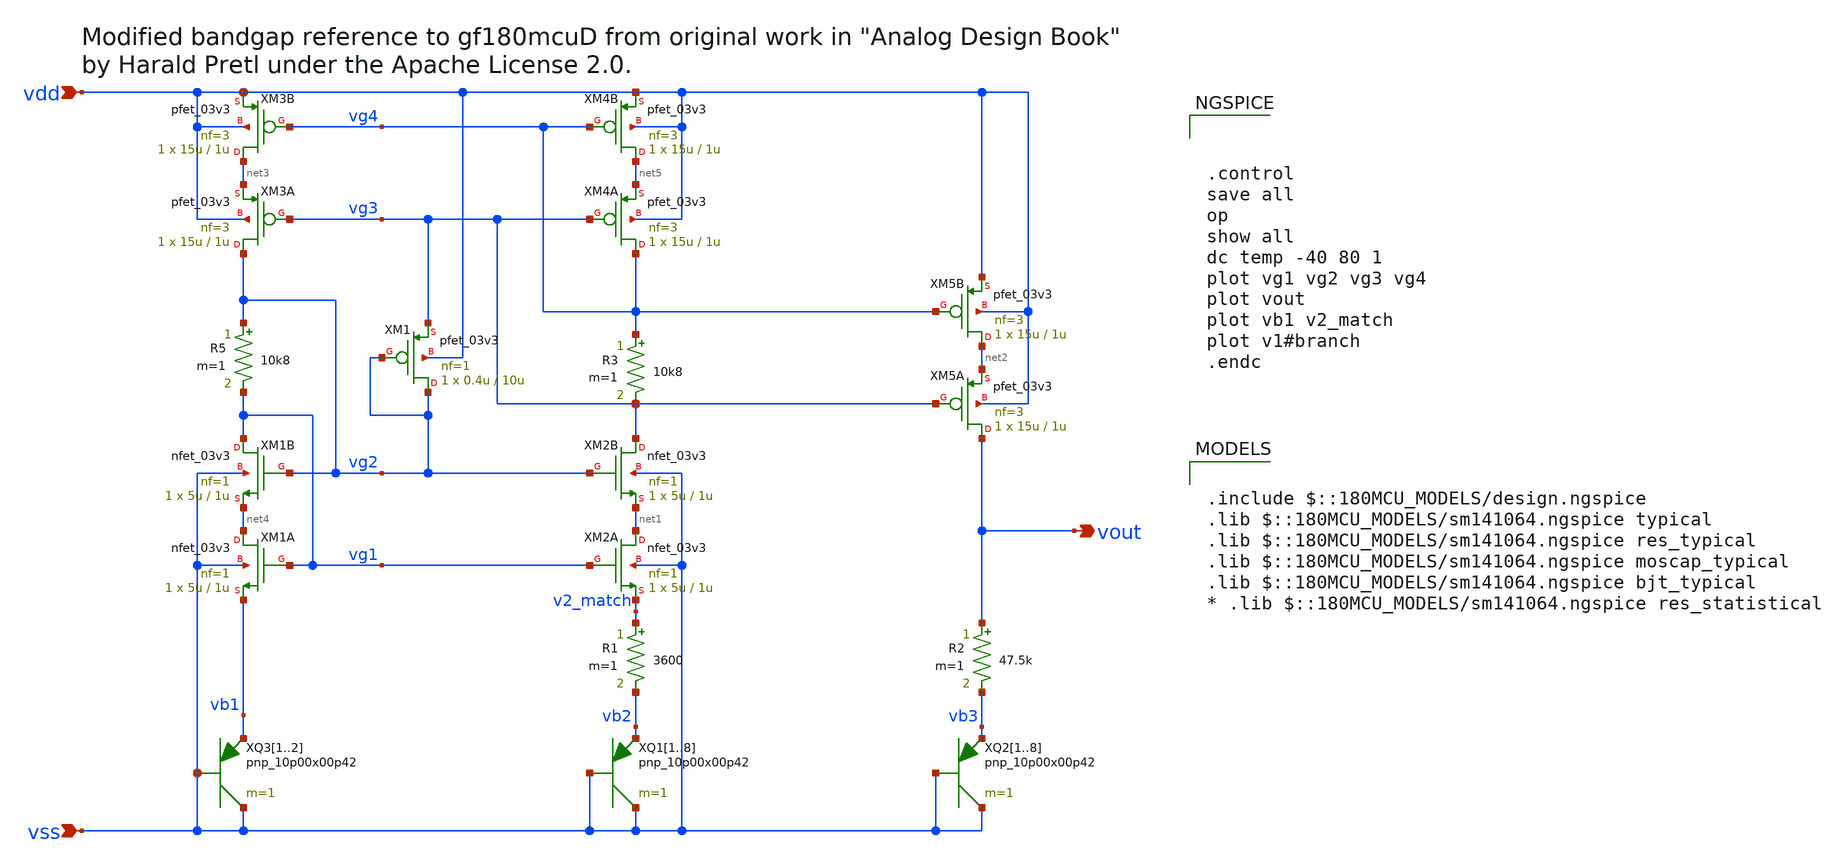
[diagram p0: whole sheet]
** sch_path: designs/switch_matrix_gf180mcu_9t5v0-main/designs/libs/core_analog/vref/voltage_reference.sch
* by Harald Pretl under the Apache License 2.0.
**.subckt voltage_reference vdd vout vss
*.ipin vdd
*.opin vout
*.ipin vss
XM1B vg1 vg2 net4 vss nfet_03v3 L=1u W=5u nf=1 ad='int((nf+1)/2) * W/nf * 0.18u' as='int((nf+2)/2) * W/nf * 0.18u'
+ pd='2*int((nf+1)/2) * (W/nf + 0.18u)' ps='2*int((nf+2)/2) * (W/nf + 0.18u)' nrd='0.18u / W' nrs='0.18u / W'
+ sa=0 sb=0 sd=0 m=1
XM1A net4 vg1 vb1 vss nfet_03v3 L=1u W=5u nf=1 ad='int((nf+1)/2) * W/nf * 0.18u' as='int((nf+2)/2) * W/nf * 0.18u'
+ pd='2*int((nf+1)/2) * (W/nf + 0.18u)' ps='2*int((nf+2)/2) * (W/nf + 0.18u)' nrd='0.18u / W' nrs='0.18u / W'
+ sa=0 sb=0 sd=0 m=1
XM2B vg3 vg2 net1 vss nfet_03v3 L=1u W=5u nf=1 ad='int((nf+1)/2) * W/nf * 0.18u' as='int((nf+2)/2) * W/nf * 0.18u'
+ pd='2*int((nf+1)/2) * (W/nf + 0.18u)' ps='2*int((nf+2)/2) * (W/nf + 0.18u)' nrd='0.18u / W' nrs='0.18u / W'
+ sa=0 sb=0 sd=0 m=1
XM2A net1 vg1 v2_match vss nfet_03v3 L=1u W=5u nf=1 ad='int((nf+1)/2) * W/nf * 0.18u' as='int((nf+2)/2) * W/nf * 0.18u'
+ pd='2*int((nf+1)/2) * (W/nf + 0.18u)' ps='2*int((nf+2)/2) * (W/nf + 0.18u)' nrd='0.18u / W' nrs='0.18u / W'
+ sa=0 sb=0 sd=0 m=1
XM4A vg4 vg3 net5 vdd pfet_03v3 L=1u W=15u nf=3 ad='int((nf+1)/2) * W/nf * 0.18u' as='int((nf+2)/2) * W/nf * 0.18u'
+ pd='2*int((nf+1)/2) * (W/nf + 0.18u)' ps='2*int((nf+2)/2) * (W/nf + 0.18u)' nrd='0.18u / W' nrs='0.18u / W'
+ sa=0 sb=0 sd=0 m=1
XM4B net5 vg4 vdd vdd pfet_03v3 L=1u W=15u nf=3 ad='int((nf+1)/2) * W/nf * 0.18u' as='int((nf+2)/2) * W/nf * 0.18u'
+ pd='2*int((nf+1)/2) * (W/nf + 0.18u)' ps='2*int((nf+2)/2) * (W/nf + 0.18u)' nrd='0.18u / W' nrs='0.18u / W'
+ sa=0 sb=0 sd=0 m=1
XM3A vg2 vg3 net3 vdd pfet_03v3 L=1u W=15u nf=3 ad='int((nf+1)/2) * W/nf * 0.18u' as='int((nf+2)/2) * W/nf * 0.18u'
+ pd='2*int((nf+1)/2) * (W/nf + 0.18u)' ps='2*int((nf+2)/2) * (W/nf + 0.18u)' nrd='0.18u / W' nrs='0.18u / W'
+ sa=0 sb=0 sd=0 m=1
XM3B net3 vg4 vdd vdd pfet_03v3 L=1u W=15u nf=3 ad='int((nf+1)/2) * W/nf * 0.18u' as='int((nf+2)/2) * W/nf * 0.18u'
+ pd='2*int((nf+1)/2) * (W/nf + 0.18u)' ps='2*int((nf+2)/2) * (W/nf + 0.18u)' nrd='0.18u / W' nrs='0.18u / W'
+ sa=0 sb=0 sd=0 m=1
XM5A vout vg3 net2 vdd pfet_03v3 L=1u W=15u nf=3 ad='int((nf+1)/2) * W/nf * 0.18u' as='int((nf+2)/2) * W/nf * 0.18u'
+ pd='2*int((nf+1)/2) * (W/nf + 0.18u)' ps='2*int((nf+2)/2) * (W/nf + 0.18u)' nrd='0.18u / W' nrs='0.18u / W'
+ sa=0 sb=0 sd=0 m=1
XM5B net2 vg4 vdd vdd pfet_03v3 L=1u W=15u nf=3 ad='int((nf+1)/2) * W/nf * 0.18u' as='int((nf+2)/2) * W/nf * 0.18u'
+ pd='2*int((nf+1)/2) * (W/nf + 0.18u)' ps='2*int((nf+2)/2) * (W/nf + 0.18u)' nrd='0.18u / W' nrs='0.18u / W'
+ sa=0 sb=0 sd=0 m=1
XQ11 vss vss vb2 pnp_10p00x00p42 m=1 par=1
XQ12 vss vss vb2 pnp_10p00x00p42 m=1 par=1
XQ13 vss vss vb2 pnp_10p00x00p42 m=1 par=1
XQ14 vss vss vb2 pnp_10p00x00p42 m=1 par=1
XQ15 vss vss vb2 pnp_10p00x00p42 m=1 par=1
XQ16 vss vss vb2 pnp_10p00x00p42 m=1 par=1
XQ17 vss vss vb2 pnp_10p00x00p42 m=1 par=1
XQ18 vss vss vb2 pnp_10p00x00p42 m=1 par=1
XQ21 vss vss vb3 pnp_10p00x00p42 m=1 par=1
XQ22 vss vss vb3 pnp_10p00x00p42 m=1 par=1
XQ23 vss vss vb3 pnp_10p00x00p42 m=1 par=1
XQ24 vss vss vb3 pnp_10p00x00p42 m=1 par=1
XQ25 vss vss vb3 pnp_10p00x00p42 m=1 par=1
XQ26 vss vss vb3 pnp_10p00x00p42 m=1 par=1
XQ27 vss vss vb3 pnp_10p00x00p42 m=1 par=1
XQ28 vss vss vb3 pnp_10p00x00p42 m=1 par=1
XQ31 vss vss vb1 pnp_10p00x00p42 m=1 par=1
XQ32 vss vss vb1 pnp_10p00x00p42 m=1 par=1
R5 vg2 vg1 10k8 m=1
R3 vg4 vg3 10k8 m=1
R2 vout vb3 47.5k m=1
R1 v2_match vb2 3600 m=1
XM1 vg2 vg2 vg3 vdd pfet_03v3 L=10u W=0.4u nf=1 ad='int((nf+1)/2) * W/nf * 0.18u' as='int((nf+2)/2) * W/nf * 0.18u'
+ pd='2*int((nf+1)/2) * (W/nf + 0.18u)' ps='2*int((nf+2)/2) * (W/nf + 0.18u)' nrd='0.18u / W' nrs='0.18u / W'
+ sa=0 sb=0 sd=0 m=1
**** begin user architecture code



.control
save all
op
show all
dc temp -40 80 1
plot vg1 vg2 vg3 vg4
plot vout
plot vb1 v2_match
plot v1#branch
.endc



.include $::180MCU_MODELS/design.ngspice
.lib $::180MCU_MODELS/sm141064.ngspice typical
.lib $::180MCU_MODELS/sm141064.ngspice res_typical
.lib $::180MCU_MODELS/sm141064.ngspice moscap_typical
.lib $::180MCU_MODELS/sm141064.ngspice bjt_typical
* .lib $::180MCU_MODELS/sm141064.ngspice res_statistical

**** end user architecture code
**.ends
.end
